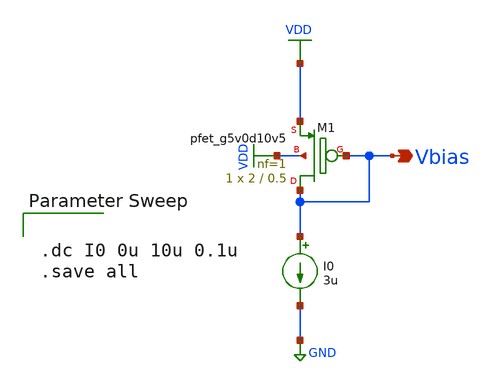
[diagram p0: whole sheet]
** sch_path: Abishek_Sam_group/template/current_mirror.sch
**.subckt current_mirror Vbias
*.opin Vbias
XM1 Vbias Vbias VDD VDD sky130_fd_pr__pfet_g5v0d10v5 L=0.5 W=2 nf=1 ad='int((nf+1)/2) * W/nf * 0.29'
+ as='int((nf+2)/2) * W/nf * 0.29' pd='2*int((nf+1)/2) * (W/nf + 0.29)' ps='2*int((nf+2)/2) * (W/nf + 0.29)'
+ nrd='0.29 / W' nrs='0.29 / W' sa=0 sb=0 sd=0 mult=1 m=1
I0 Vbias GND 3u
**** begin user architecture code

.lib $::SKYWATER_MODELS/sky130.lib.spice tt



.dc I0 0u 10u 0.1u
.save all


**** end user architecture code
**.ends
.GLOBAL GND
.GLOBAL VDD
.end
